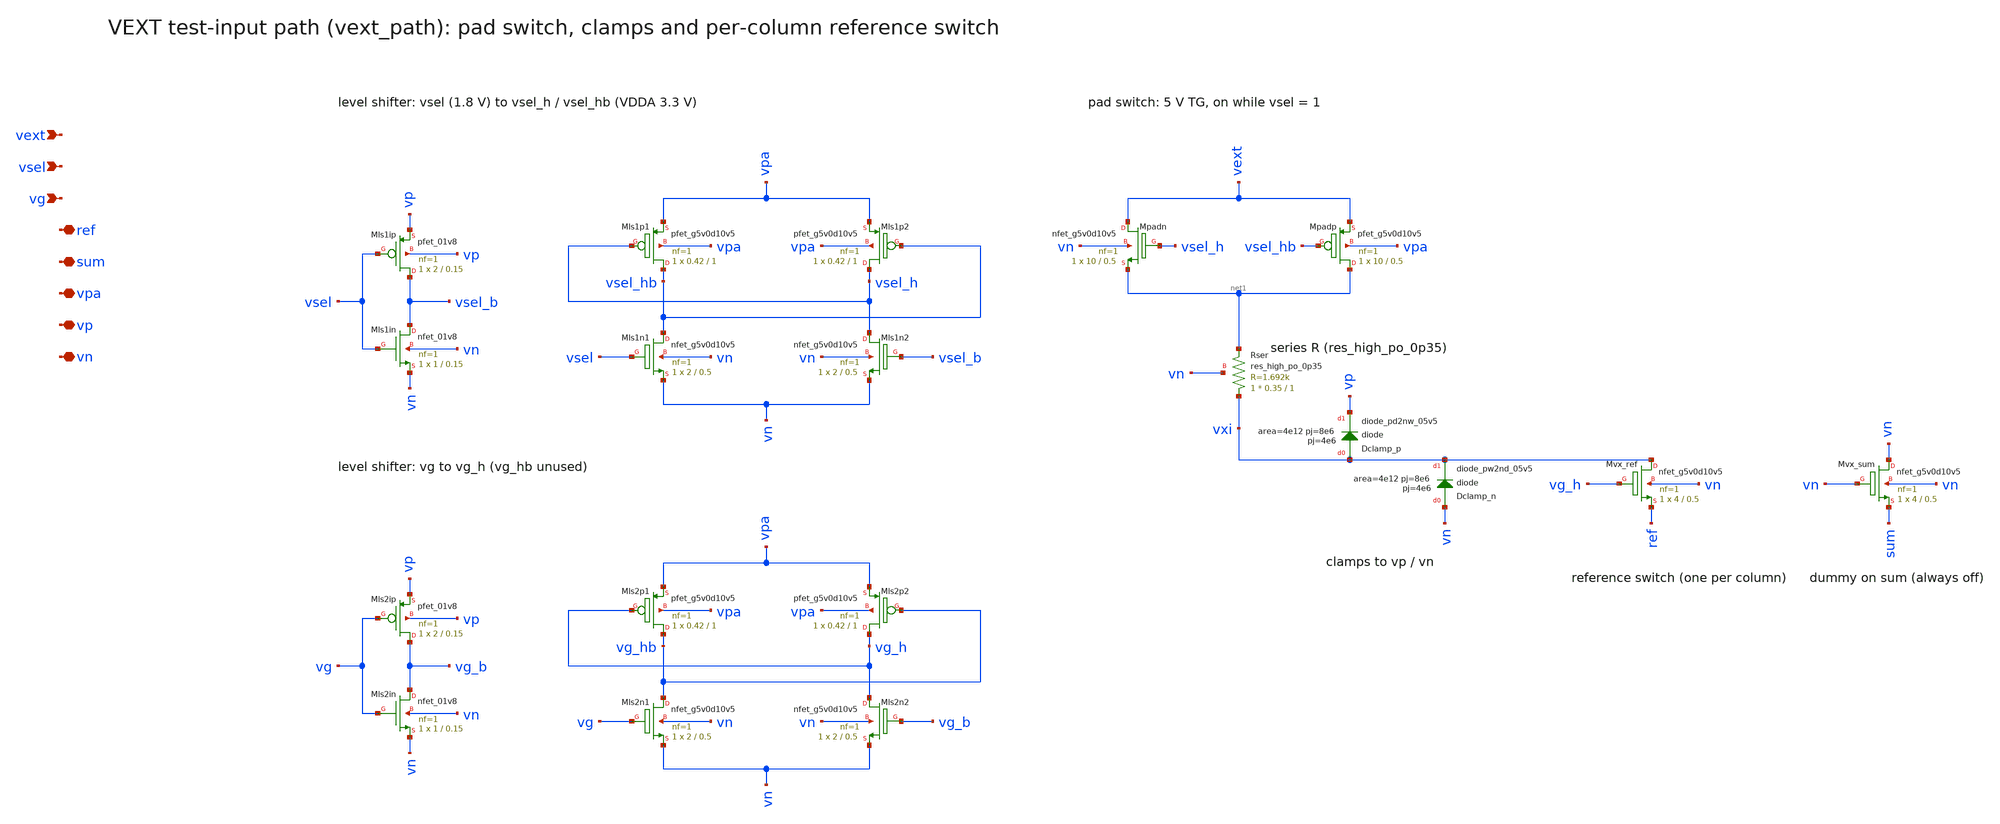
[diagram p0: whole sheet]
** sch_path: xschem/vext_path.sch
**.subckt vext_path vext vsel vg ref sum vpa vp vn
*.ipin vext
*.ipin vsel
*.ipin vg
*.iopin ref
*.iopin sum
*.iopin vpa
*.iopin vp
*.iopin vn
XMls1ip vsel_b vsel vp vp sky130_fd_pr__pfet_01v8 L=0.15 W=2 nf=1 ad='int((nf+1)/2) * W/nf * 0.29' as='int((nf+2)/2) * W/nf * 0.29'
+ pd='2*int((nf+1)/2) * (W/nf + 0.29)' ps='2*int((nf+2)/2) * (W/nf + 0.29)' nrd=0 nrs=0 sa=0 sb=0 sd=0
+ mult=1 m=1
XMls1in vsel_b vsel vn vn sky130_fd_pr__nfet_01v8 L=0.15 W=1 nf=1 ad='int((nf+1)/2) * W/nf * 0.29' as='int((nf+2)/2) * W/nf * 0.29'
+ pd='2*int((nf+1)/2) * (W/nf + 0.29)' ps='2*int((nf+2)/2) * (W/nf + 0.29)' nrd=0 nrs=0 sa=0 sb=0 sd=0
+ mult=1 m=1
XMls1p1 vsel_hb vsel_h vpa vpa sky130_fd_pr__pfet_g5v0d10v5 L=1 W=0.42 nf=1 ad='int((nf+1)/2) * W/nf * 0.29'
+ as='int((nf+2)/2) * W/nf * 0.29' pd='2*int((nf+1)/2) * (W/nf + 0.29)' ps='2*int((nf+2)/2) * (W/nf + 0.29)'
+ nrd=0 nrs=0 sa=0 sb=0 sd=0 mult=1 m=1
XMls1p2 vsel_h vsel_hb vpa vpa sky130_fd_pr__pfet_g5v0d10v5 L=1 W=0.42 nf=1 ad='int((nf+1)/2) * W/nf * 0.29'
+ as='int((nf+2)/2) * W/nf * 0.29' pd='2*int((nf+1)/2) * (W/nf + 0.29)' ps='2*int((nf+2)/2) * (W/nf + 0.29)'
+ nrd=0 nrs=0 sa=0 sb=0 sd=0 mult=1 m=1
XMls1n1 vsel_hb vsel vn vn sky130_fd_pr__nfet_g5v0d10v5 L=0.5 W=2 nf=1 ad='int((nf+1)/2) * W/nf * 0.29'
+ as='int((nf+2)/2) * W/nf * 0.29' pd='2*int((nf+1)/2) * (W/nf + 0.29)' ps='2*int((nf+2)/2) * (W/nf + 0.29)'
+ nrd=0 nrs=0 sa=0 sb=0 sd=0 mult=1 m=1
XMls1n2 vsel_h vsel_b vn vn sky130_fd_pr__nfet_g5v0d10v5 L=0.5 W=2 nf=1 ad='int((nf+1)/2) * W/nf * 0.29'
+ as='int((nf+2)/2) * W/nf * 0.29' pd='2*int((nf+1)/2) * (W/nf + 0.29)' ps='2*int((nf+2)/2) * (W/nf + 0.29)'
+ nrd=0 nrs=0 sa=0 sb=0 sd=0 mult=1 m=1
XMls2ip vg_b vg vp vp sky130_fd_pr__pfet_01v8 L=0.15 W=2 nf=1 ad='int((nf+1)/2) * W/nf * 0.29' as='int((nf+2)/2) * W/nf * 0.29'
+ pd='2*int((nf+1)/2) * (W/nf + 0.29)' ps='2*int((nf+2)/2) * (W/nf + 0.29)' nrd=0 nrs=0 sa=0 sb=0 sd=0
+ mult=1 m=1
XMls2in vg_b vg vn vn sky130_fd_pr__nfet_01v8 L=0.15 W=1 nf=1 ad='int((nf+1)/2) * W/nf * 0.29' as='int((nf+2)/2) * W/nf * 0.29'
+ pd='2*int((nf+1)/2) * (W/nf + 0.29)' ps='2*int((nf+2)/2) * (W/nf + 0.29)' nrd=0 nrs=0 sa=0 sb=0 sd=0
+ mult=1 m=1
XMls2p1 vg_hb vg_h vpa vpa sky130_fd_pr__pfet_g5v0d10v5 L=1 W=0.42 nf=1 ad='int((nf+1)/2) * W/nf * 0.29'
+ as='int((nf+2)/2) * W/nf * 0.29' pd='2*int((nf+1)/2) * (W/nf + 0.29)' ps='2*int((nf+2)/2) * (W/nf + 0.29)'
+ nrd=0 nrs=0 sa=0 sb=0 sd=0 mult=1 m=1
XMls2p2 vg_h vg_hb vpa vpa sky130_fd_pr__pfet_g5v0d10v5 L=1 W=0.42 nf=1 ad='int((nf+1)/2) * W/nf * 0.29'
+ as='int((nf+2)/2) * W/nf * 0.29' pd='2*int((nf+1)/2) * (W/nf + 0.29)' ps='2*int((nf+2)/2) * (W/nf + 0.29)'
+ nrd=0 nrs=0 sa=0 sb=0 sd=0 mult=1 m=1
XMls2n1 vg_hb vg vn vn sky130_fd_pr__nfet_g5v0d10v5 L=0.5 W=2 nf=1 ad='int((nf+1)/2) * W/nf * 0.29' as='int((nf+2)/2) * W/nf * 0.29'
+ pd='2*int((nf+1)/2) * (W/nf + 0.29)' ps='2*int((nf+2)/2) * (W/nf + 0.29)' nrd=0 nrs=0 sa=0 sb=0 sd=0
+ mult=1 m=1
XMls2n2 vg_h vg_b vn vn sky130_fd_pr__nfet_g5v0d10v5 L=0.5 W=2 nf=1 ad='int((nf+1)/2) * W/nf * 0.29'
+ as='int((nf+2)/2) * W/nf * 0.29' pd='2*int((nf+1)/2) * (W/nf + 0.29)' ps='2*int((nf+2)/2) * (W/nf + 0.29)'
+ nrd=0 nrs=0 sa=0 sb=0 sd=0 mult=1 m=1
XMpadn vext vsel_h net1 vn sky130_fd_pr__nfet_g5v0d10v5 L=0.5 W=10 nf=1 ad='int((nf+1)/2) * W/nf * 0.29'
+ as='int((nf+2)/2) * W/nf * 0.29' pd='2*int((nf+1)/2) * (W/nf + 0.29)' ps='2*int((nf+2)/2) * (W/nf + 0.29)'
+ nrd=0 nrs=0 sa=0 sb=0 sd=0 mult=1 m=1
XMpadp net1 vsel_hb vext vpa sky130_fd_pr__pfet_g5v0d10v5 L=0.5 W=10 nf=1 ad='int((nf+1)/2) * W/nf * 0.29'
+ as='int((nf+2)/2) * W/nf * 0.29' pd='2*int((nf+1)/2) * (W/nf + 0.29)' ps='2*int((nf+2)/2) * (W/nf + 0.29)'
+ nrd=0 nrs=0 sa=0 sb=0 sd=0 mult=1 m=1
XRser vxi net1 vn sky130_fd_pr__res_high_po_0p35 L=1 mult=1 m=1
XDclamp_p vxi vp sky130_fd_pr__diode_pd2nw_05v5 area=4e12 pj=8e6 pj=4e6
XDclamp_n vn vxi sky130_fd_pr__diode_pw2nd_05v5 area=4e12 pj=8e6 pj=4e6
XMvx_ref vxi vg_h ref vn sky130_fd_pr__nfet_g5v0d10v5 L=0.5 W=4 nf=1 ad='int((nf+1)/2) * W/nf * 0.29'
+ as='int((nf+2)/2) * W/nf * 0.29' pd='2*int((nf+1)/2) * (W/nf + 0.29)' ps='2*int((nf+2)/2) * (W/nf + 0.29)'
+ nrd=0 nrs=0 sa=0 sb=0 sd=0 mult=1 m=1
XMvx_sum vn vn sum vn sky130_fd_pr__nfet_g5v0d10v5 L=0.5 W=4 nf=1 ad='int((nf+1)/2) * W/nf * 0.29' as='int((nf+2)/2) * W/nf * 0.29'
+ pd='2*int((nf+1)/2) * (W/nf + 0.29)' ps='2*int((nf+2)/2) * (W/nf + 0.29)' nrd=0 nrs=0 sa=0 sb=0 sd=0
+ mult=1 m=1
**.ends
.end
